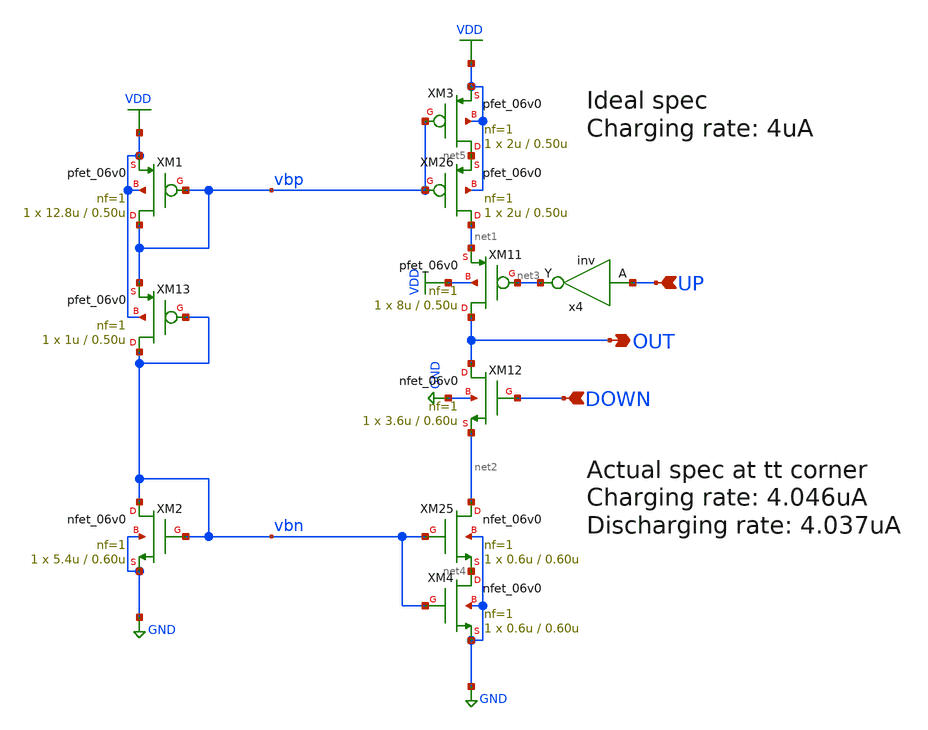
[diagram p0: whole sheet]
** sch_path: cp.sch
**.subckt cp OUT UP DOWN
*.opin OUT
*.ipin UP
*.ipin DOWN
XM11 OUT net3 net1 VDD pfet_06v0 L=0.50u W=8u nf=1 ad='int((nf+1)/2) * W/nf * 0.18u' as='int((nf+2)/2) * W/nf * 0.18u'
+ pd='2*int((nf+1)/2) * (W/nf + 0.18u)' ps='2*int((nf+2)/2) * (W/nf + 0.18u)' nrd='0.18u / W' nrs='0.18u / W'
+ sa=0 sb=0 sd=0 m=1
XM12 OUT DOWN net2 GND nfet_06v0 L=0.60u W=3.6u nf=1 ad='int((nf+1)/2) * W/nf * 0.18u' as='int((nf+2)/2) * W/nf * 0.18u'
+ pd='2*int((nf+1)/2) * (W/nf + 0.18u)' ps='2*int((nf+2)/2) * (W/nf + 0.18u)' nrd='0.18u / W' nrs='0.18u / W'
+ sa=0 sb=0 sd=0 m=1
x4 UP net3 inv
XM1 vbp vbp VDD VDD pfet_06v0 L=0.50u W=12.8u nf=1 ad='int((nf+1)/2) * W/nf * 0.18u' as='int((nf+2)/2) * W/nf * 0.18u'
+ pd='2*int((nf+1)/2) * (W/nf + 0.18u)' ps='2*int((nf+2)/2) * (W/nf + 0.18u)' nrd='0.18u / W' nrs='0.18u / W'
+ sa=0 sb=0 sd=0 m=1
XM2 vbn vbn GND GND nfet_06v0 L=0.60u W=5.4u nf=1 ad='int((nf+1)/2) * W/nf * 0.18u' as='int((nf+2)/2) * W/nf * 0.18u'
+ pd='2*int((nf+1)/2) * (W/nf + 0.18u)' ps='2*int((nf+2)/2) * (W/nf + 0.18u)' nrd='0.18u / W' nrs='0.18u / W'
+ sa=0 sb=0 sd=0 m=1
XM13 vbn vbn vbp VDD pfet_06v0 L=0.50u W=1u nf=1 ad='int((nf+1)/2) * W/nf * 0.18u' as='int((nf+2)/2) * W/nf * 0.18u'
+ pd='2*int((nf+1)/2) * (W/nf + 0.18u)' ps='2*int((nf+2)/2) * (W/nf + 0.18u)' nrd='0.18u / W' nrs='0.18u / W'
+ sa=0 sb=0 sd=0 m=1
XM4 net4 vbn GND GND nfet_06v0 L=0.60u W=0.6u nf=1 ad='int((nf+1)/2) * W/nf * 0.18u' as='int((nf+2)/2) * W/nf * 0.18u'
+ pd='2*int((nf+1)/2) * (W/nf + 0.18u)' ps='2*int((nf+2)/2) * (W/nf + 0.18u)' nrd='0.18u / W' nrs='0.18u / W'
+ sa=0 sb=0 sd=0 m=1
XM25 net2 vbn net4 GND nfet_06v0 L=0.60u W=0.6u nf=1 ad='int((nf+1)/2) * W/nf * 0.18u' as='int((nf+2)/2) * W/nf * 0.18u'
+ pd='2*int((nf+1)/2) * (W/nf + 0.18u)' ps='2*int((nf+2)/2) * (W/nf + 0.18u)' nrd='0.18u / W' nrs='0.18u / W'
+ sa=0 sb=0 sd=0 m=1
XM3 net5 vbp VDD VDD pfet_06v0 L=0.50u W=2u nf=1 ad='int((nf+1)/2) * W/nf * 0.18u' as='int((nf+2)/2) * W/nf * 0.18u'
+ pd='2*int((nf+1)/2) * (W/nf + 0.18u)' ps='2*int((nf+2)/2) * (W/nf + 0.18u)' nrd='0.18u / W' nrs='0.18u / W'
+ sa=0 sb=0 sd=0 m=1
XM26 net1 vbp net5 VDD pfet_06v0 L=0.50u W=2u nf=1 ad='int((nf+1)/2) * W/nf * 0.18u' as='int((nf+2)/2) * W/nf * 0.18u'
+ pd='2*int((nf+1)/2) * (W/nf + 0.18u)' ps='2*int((nf+2)/2) * (W/nf + 0.18u)' nrd='0.18u / W' nrs='0.18u / W'
+ sa=0 sb=0 sd=0 m=1
**.ends

* expanding   symbol:  inv.sym # of pins=2
** sym_path: inv.sym
** sch_path: inv.sch
.subckt inv A Y
*.opin Y
*.ipin A
XM1 Y A VDD VDD pfet_06v0 L=0.50u W=2u nf=1 ad='int((nf+1)/2) * W/nf * 0.18u' as='int((nf+2)/2) * W/nf * 0.18u'
+ pd='2*int((nf+1)/2) * (W/nf + 0.18u)' ps='2*int((nf+2)/2) * (W/nf + 0.18u)' nrd='0.18u / W' nrs='0.18u / W'
+ sa=0 sb=0 sd=0 m=1
XM2 Y A GND GND nfet_06v0 L=0.60u W=0.9u nf=1 ad='int((nf+1)/2) * W/nf * 0.18u' as='int((nf+2)/2) * W/nf * 0.18u'
+ pd='2*int((nf+1)/2) * (W/nf + 0.18u)' ps='2*int((nf+2)/2) * (W/nf + 0.18u)' nrd='0.18u / W' nrs='0.18u / W'
+ sa=0 sb=0 sd=0 m=1
.ends

.GLOBAL VDD
.GLOBAL GND
.end
